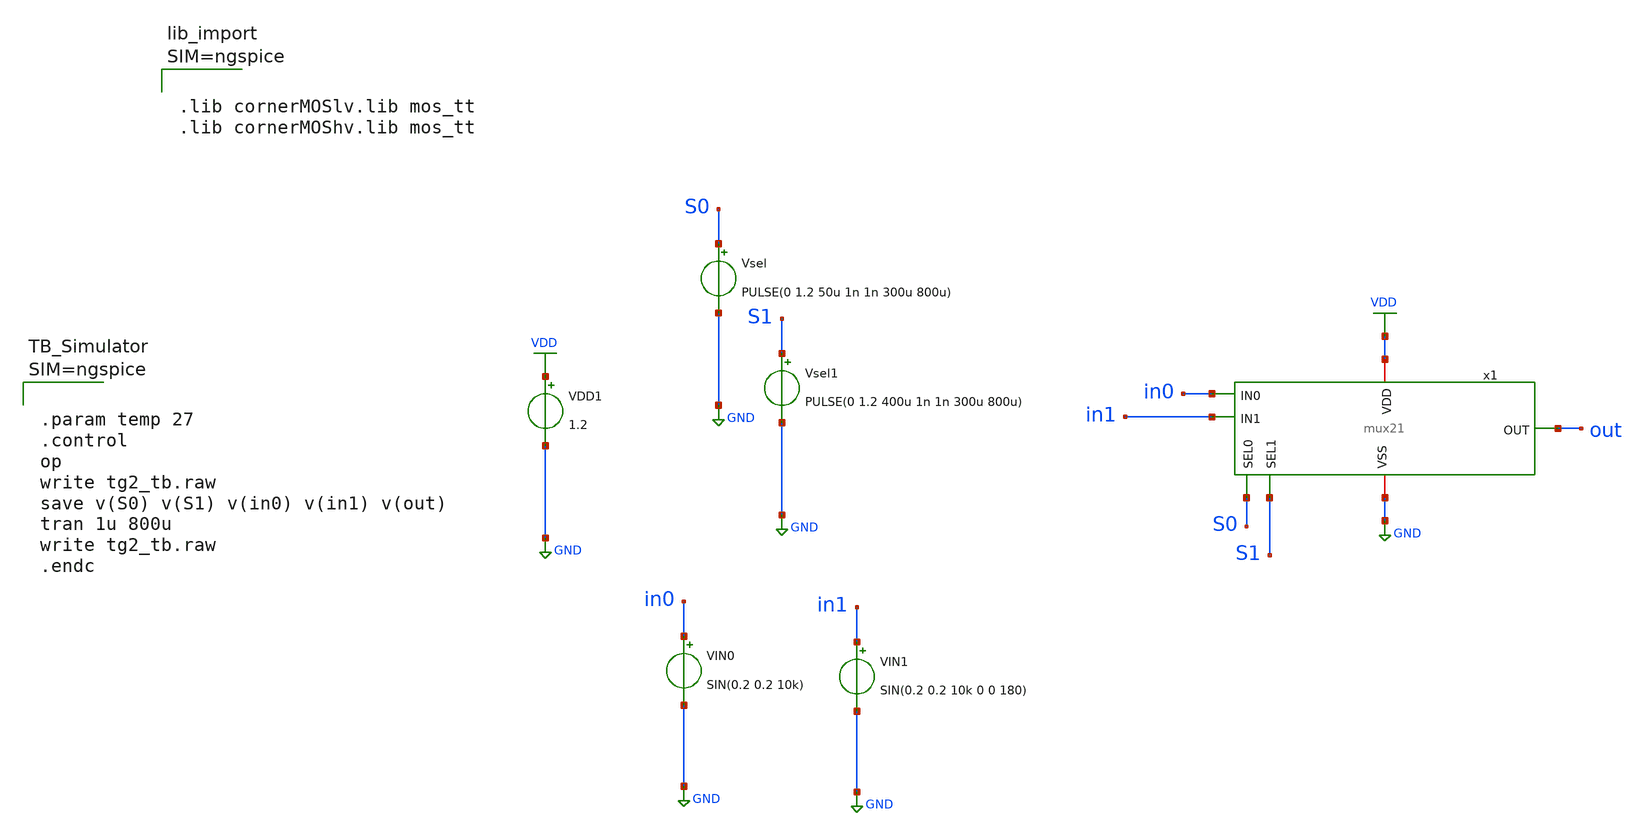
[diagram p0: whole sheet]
** sch_path: xschem/ncs-dpi-adexp/xschem/mux_tb.sch
**.subckt mux_tb
VDD1 VDD GND 1.2
VIN0 in0 GND SIN(0.2 0.2 10k)
Vsel S0 GND PULSE(0 1.2 50u 1n 1n 300u 800u)
VIN1 in1 GND SIN(0.2 0.2 10k 0 0 180)
Vsel1 S1 GND PULSE(0 1.2 400u 1n 1n 300u 800u)
x1 VDD GND in0 in1 S0 S1 out mux21
**** begin user architecture code



.lib cornerMOSlv.lib mos_tt
.lib cornerMOShv.lib mos_tt





.param temp 27
.control
op
write tg2_tb.raw
save v(S0) v(S1) v(in0) v(in1) v(out)
tran 1u 800u
write tg2_tb.raw
.endc



**** end user architecture code
**.ends
.GLOBAL GND
.GLOBAL VDD
.end
